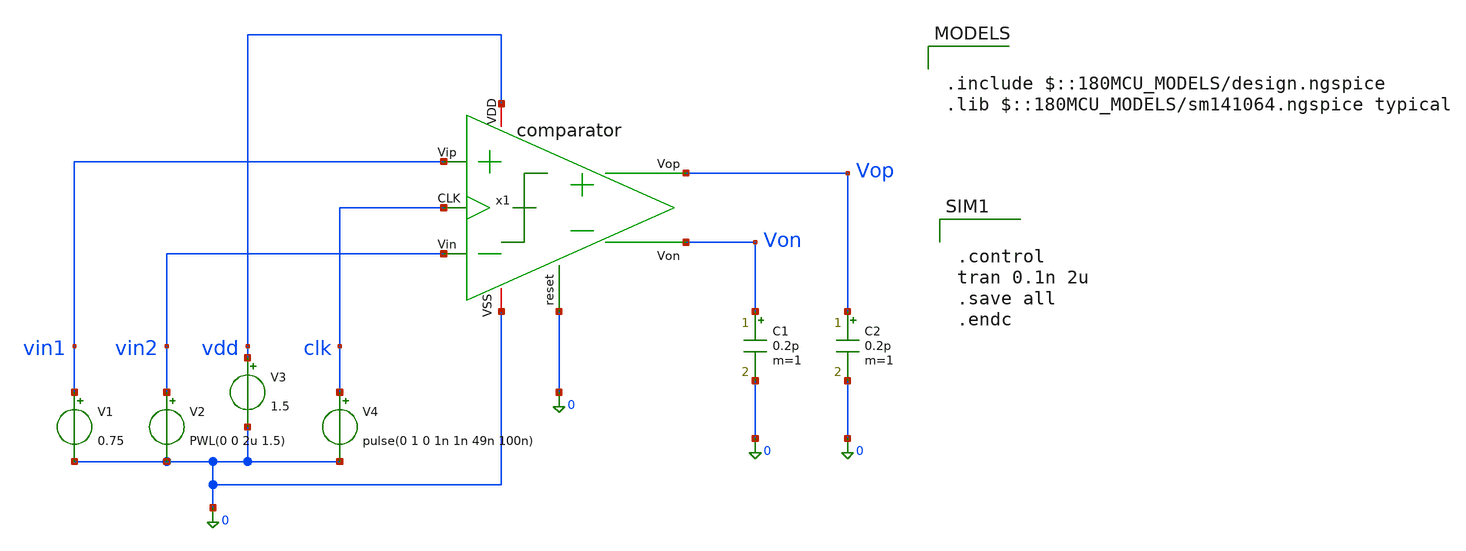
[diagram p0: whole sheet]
** sch_path: designs/DS_modulator/comparator/xschem/comparator_TB_DCIN.sch
**.subckt comparator_TB_DCIN
V1 vin1 0 0.75
V2 vin2 0 PWL(0 0 2u 1.5)
V3 vdd 0 1.5
V4 clk 0 pulse(0 1 0 1n 1n 49n 100n)
x1 vdd clk Vop 0 Von vin1 vin2 0 comparator
C1 Von 0 0.2p m=1
C2 Vop 0 0.2p m=1
**** begin user architecture code


.control
tran 0.1n 2u
.save all
.endc


.include $::180MCU_MODELS/design.ngspice
.lib $::180MCU_MODELS/sm141064.ngspice typical

**** end user architecture code
**.ends
.end
